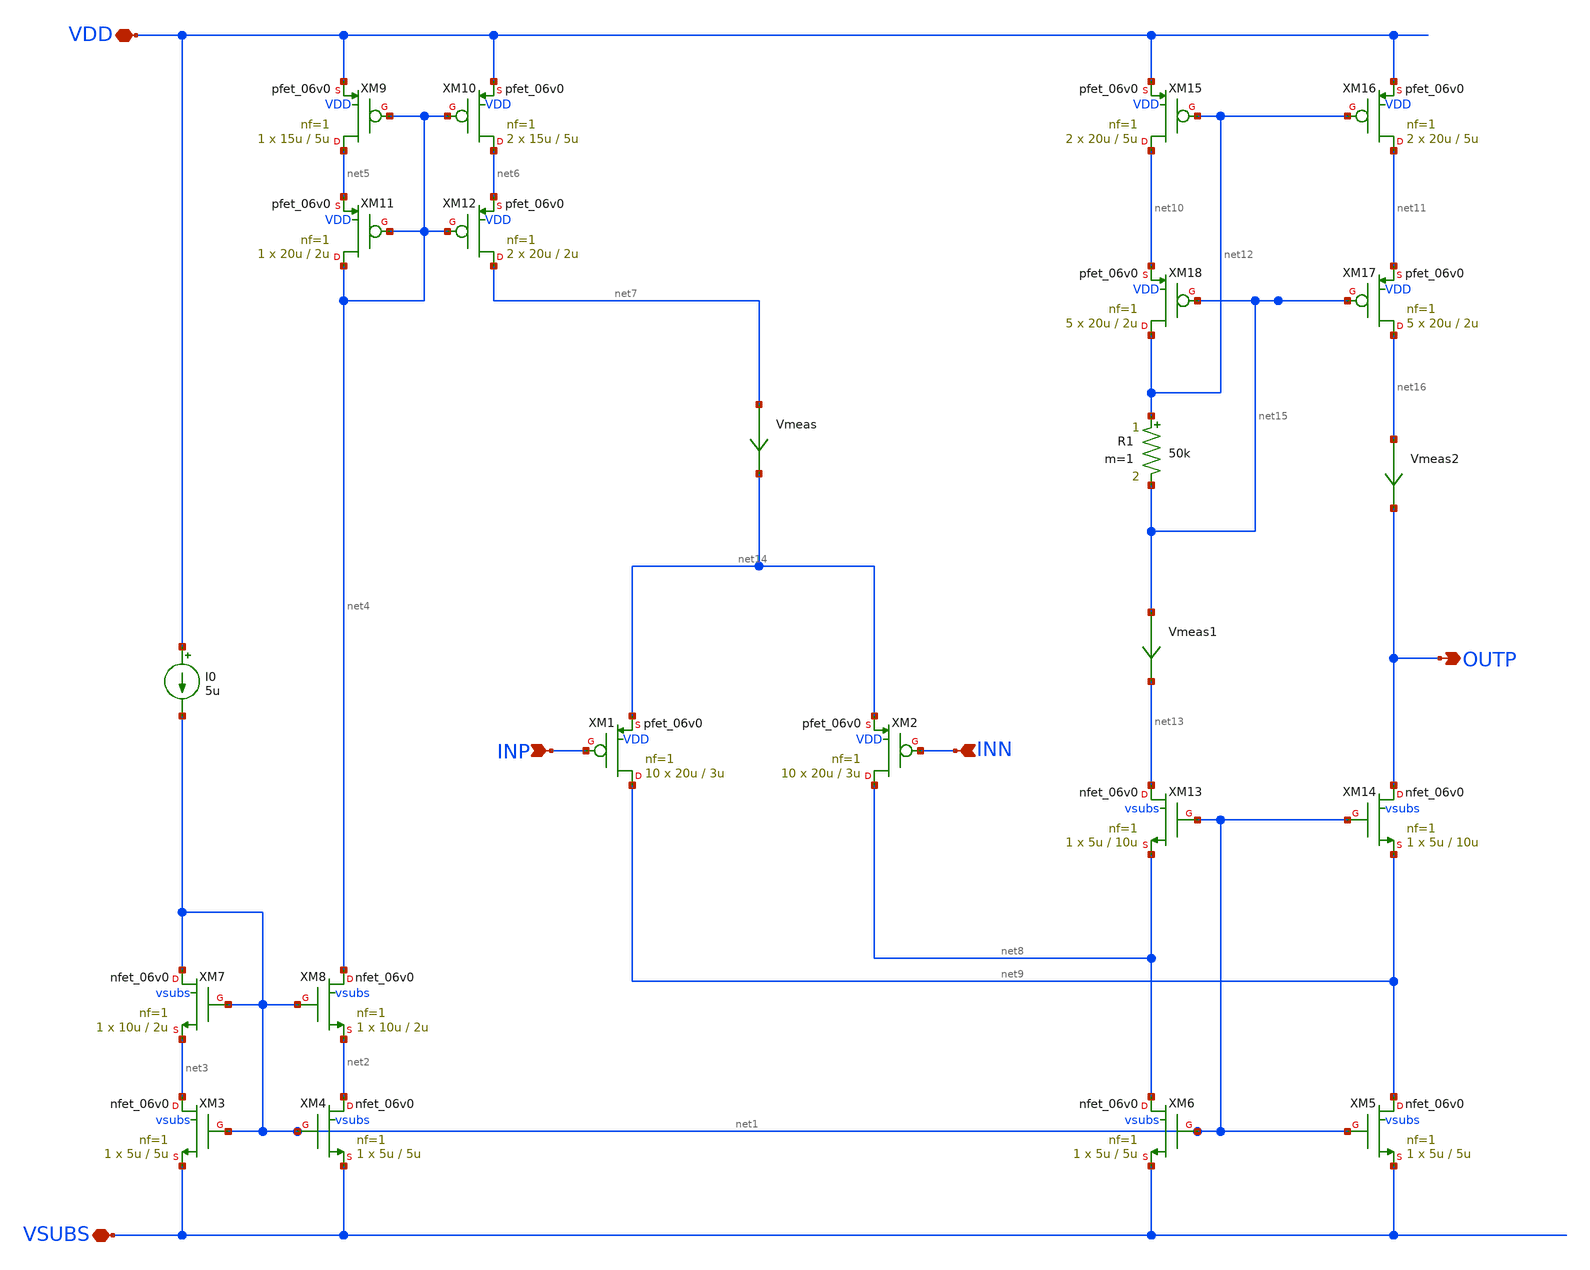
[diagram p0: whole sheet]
** sch_path: xschem/ip_amplifier.sch
**.subckt ip_amplifier VDD VSUBS INP INN OUTP
*.iopin VDD
*.iopin VSUBS
*.ipin INP
*.ipin INN
*.opin OUTP
XM1 net9 INP net14 VDD pfet_06v0 L=3u W=20u nf=1 ad='int((nf+1)/2) * W/nf * 0.18u' as='int((nf+2)/2) * W/nf * 0.18u'
+ pd='2*int((nf+1)/2) * (W/nf + 0.18u)' ps='2*int((nf+2)/2) * (W/nf + 0.18u)' nrd='0.18u / W' nrs='0.18u / W'
+ sa=0 sb=0 sd=0 m=10 par=10
XM2 net8 INN net14 VDD pfet_06v0 L=3u W=20u nf=1 ad='int((nf+1)/2) * W/nf * 0.18u' as='int((nf+2)/2) * W/nf * 0.18u'
+ pd='2*int((nf+1)/2) * (W/nf + 0.18u)' ps='2*int((nf+2)/2) * (W/nf + 0.18u)' nrd='0.18u / W' nrs='0.18u / W'
+ sa=0 sb=0 sd=0 m=10 par=10
XM5 net9 net1 VSUBS vsubs nfet_06v0 L=5u W=5u nf=1 ad='int((nf+1)/2) * W/nf * 0.18u' as='int((nf+2)/2) * W/nf * 0.18u'
+ pd='2*int((nf+1)/2) * (W/nf + 0.18u)' ps='2*int((nf+2)/2) * (W/nf + 0.18u)' nrd='0.18u / W' nrs='0.18u / W'
+ sa=0 sb=0 sd=0 m=1 par=1
XM6 net8 net1 VSUBS vsubs nfet_06v0 L=5u W=5u nf=1 ad='int((nf+1)/2) * W/nf * 0.18u' as='int((nf+2)/2) * W/nf * 0.18u'
+ pd='2*int((nf+1)/2) * (W/nf + 0.18u)' ps='2*int((nf+2)/2) * (W/nf + 0.18u)' nrd='0.18u / W' nrs='0.18u / W'
+ sa=0 sb=0 sd=0 m=1 par=1
XM3 net3 net1 VSUBS vsubs nfet_06v0 L=5u W=5u nf=1 ad='int((nf+1)/2) * W/nf * 0.18u' as='int((nf+2)/2) * W/nf * 0.18u'
+ pd='2*int((nf+1)/2) * (W/nf + 0.18u)' ps='2*int((nf+2)/2) * (W/nf + 0.18u)' nrd='0.18u / W' nrs='0.18u / W'
+ sa=0 sb=0 sd=0 m=1 par=1
XM4 net2 net1 VSUBS vsubs nfet_06v0 L=5u W=5u nf=1 ad='int((nf+1)/2) * W/nf * 0.18u' as='int((nf+2)/2) * W/nf * 0.18u'
+ pd='2*int((nf+1)/2) * (W/nf + 0.18u)' ps='2*int((nf+2)/2) * (W/nf + 0.18u)' nrd='0.18u / W' nrs='0.18u / W'
+ sa=0 sb=0 sd=0 m=1 par=1
XM7 net1 net1 net3 vsubs nfet_06v0 L=2u W=10u nf=1 ad='int((nf+1)/2) * W/nf * 0.18u' as='int((nf+2)/2) * W/nf * 0.18u'
+ pd='2*int((nf+1)/2) * (W/nf + 0.18u)' ps='2*int((nf+2)/2) * (W/nf + 0.18u)' nrd='0.18u / W' nrs='0.18u / W'
+ sa=0 sb=0 sd=0 m=1 par=1
XM8 net4 net1 net2 vsubs nfet_06v0 L=2u W=10u nf=1 ad='int((nf+1)/2) * W/nf * 0.18u' as='int((nf+2)/2) * W/nf * 0.18u'
+ pd='2*int((nf+1)/2) * (W/nf + 0.18u)' ps='2*int((nf+2)/2) * (W/nf + 0.18u)' nrd='0.18u / W' nrs='0.18u / W'
+ sa=0 sb=0 sd=0 m=1 par=1
I0 VDD net1 5u
XM9 net5 net4 VDD VDD pfet_06v0 L=5u W=15u nf=1 ad='int((nf+1)/2) * W/nf * 0.18u' as='int((nf+2)/2) * W/nf * 0.18u'
+ pd='2*int((nf+1)/2) * (W/nf + 0.18u)' ps='2*int((nf+2)/2) * (W/nf + 0.18u)' nrd='0.18u / W' nrs='0.18u / W'
+ sa=0 sb=0 sd=0 m=1 par=1
XM10 net6 net4 VDD VDD pfet_06v0 L=5u W=15u nf=1 ad='int((nf+1)/2) * W/nf * 0.18u' as='int((nf+2)/2) * W/nf * 0.18u'
+ pd='2*int((nf+1)/2) * (W/nf + 0.18u)' ps='2*int((nf+2)/2) * (W/nf + 0.18u)' nrd='0.18u / W' nrs='0.18u / W'
+ sa=0 sb=0 sd=0 m=2 par=2
XM11 net4 net4 net5 VDD pfet_06v0 L=2u W=20u nf=1 ad='int((nf+1)/2) * W/nf * 0.18u' as='int((nf+2)/2) * W/nf * 0.18u'
+ pd='2*int((nf+1)/2) * (W/nf + 0.18u)' ps='2*int((nf+2)/2) * (W/nf + 0.18u)' nrd='0.18u / W' nrs='0.18u / W'
+ sa=0 sb=0 sd=0 m=1 par=1
XM12 net7 net4 net6 VDD pfet_06v0 L=2u W=20u nf=1 ad='int((nf+1)/2) * W/nf * 0.18u' as='int((nf+2)/2) * W/nf * 0.18u'
+ pd='2*int((nf+1)/2) * (W/nf + 0.18u)' ps='2*int((nf+2)/2) * (W/nf + 0.18u)' nrd='0.18u / W' nrs='0.18u / W'
+ sa=0 sb=0 sd=0 m=2 par=2
XM13 net13 net1 net8 vsubs nfet_06v0 L=10u W=5u nf=1 ad='int((nf+1)/2) * W/nf * 0.18u' as='int((nf+2)/2) * W/nf * 0.18u'
+ pd='2*int((nf+1)/2) * (W/nf + 0.18u)' ps='2*int((nf+2)/2) * (W/nf + 0.18u)' nrd='0.18u / W' nrs='0.18u / W'
+ sa=0 sb=0 sd=0 m=1 par=1
XM14 OUTP net1 net9 vsubs nfet_06v0 L=10u W=5u nf=1 ad='int((nf+1)/2) * W/nf * 0.18u' as='int((nf+2)/2) * W/nf * 0.18u'
+ pd='2*int((nf+1)/2) * (W/nf + 0.18u)' ps='2*int((nf+2)/2) * (W/nf + 0.18u)' nrd='0.18u / W' nrs='0.18u / W'
+ sa=0 sb=0 sd=0 m=1 par=1
XM15 net10 net12 VDD VDD pfet_06v0 L=5u W=20u nf=1 ad='int((nf+1)/2) * W/nf * 0.18u' as='int((nf+2)/2) * W/nf * 0.18u'
+ pd='2*int((nf+1)/2) * (W/nf + 0.18u)' ps='2*int((nf+2)/2) * (W/nf + 0.18u)' nrd='0.18u / W' nrs='0.18u / W'
+ sa=0 sb=0 sd=0 m=2 par=2
XM16 net11 net12 VDD VDD pfet_06v0 L=5u W=20u nf=1 ad='int((nf+1)/2) * W/nf * 0.18u' as='int((nf+2)/2) * W/nf * 0.18u'
+ pd='2*int((nf+1)/2) * (W/nf + 0.18u)' ps='2*int((nf+2)/2) * (W/nf + 0.18u)' nrd='0.18u / W' nrs='0.18u / W'
+ sa=0 sb=0 sd=0 m=2 par=2
XM17 net16 net15 net11 VDD pfet_06v0 L=2u W=20u nf=1 ad='int((nf+1)/2) * W/nf * 0.18u' as='int((nf+2)/2) * W/nf * 0.18u'
+ pd='2*int((nf+1)/2) * (W/nf + 0.18u)' ps='2*int((nf+2)/2) * (W/nf + 0.18u)' nrd='0.18u / W' nrs='0.18u / W'
+ sa=0 sb=0 sd=0 m=5 par=5
XM18 net12 net15 net10 VDD pfet_06v0 L=2u W=20u nf=1 ad='int((nf+1)/2) * W/nf * 0.18u' as='int((nf+2)/2) * W/nf * 0.18u'
+ pd='2*int((nf+1)/2) * (W/nf + 0.18u)' ps='2*int((nf+2)/2) * (W/nf + 0.18u)' nrd='0.18u / W' nrs='0.18u / W'
+ sa=0 sb=0 sd=0 m=5 par=5
Vmeas net7 net14 0
Vmeas1 net15 net13 0
Vmeas2 net16 OUTP 0
R1 net12 net15 50k m=1
**.ends
.end
